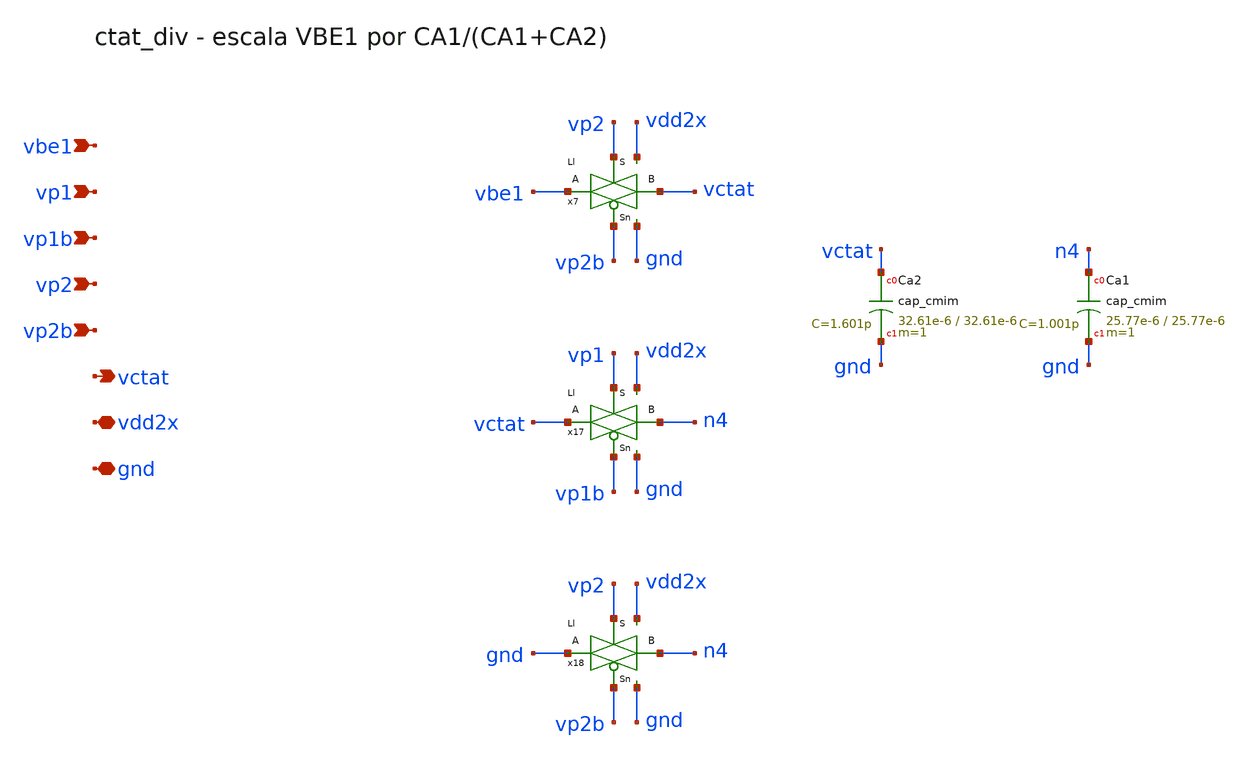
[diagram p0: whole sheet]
** sch_path: Enfoque_A/xschem/celdas/ctat_div.sch
**.subckt ctat_div vbe1 vp1 vp1b vp2 vp2b vctat vdd2x gnd
*.ipin vbe1
*.ipin vp1
*.ipin vp1b
*.ipin vp2
*.ipin vp2b
*.opin vctat
*.iopin vdd2x
*.iopin gnd
x7 vbe1 vctat vp2 vp2b vdd2x gnd Ll
x17 vctat n4 vp1 vp1b vdd2x gnd Ll
x18 gnd n4 vp2 vp2b vdd2x gnd Ll
XCa2 vctat gnd cap_cmim w=32.61e-6 l=32.61e-6 m=1 mm_ok=1
XCa1 n4 gnd cap_cmim w=25.77e-6 l=25.77e-6 m=1 mm_ok=1
**.ends

* expanding   symbol:  Enfoque_A/xschem/celdas/Ll.sym # of pins=6
** sym_path: Enfoque_A/xschem/celdas/Ll.sym
** sch_path: Enfoque_A/xschem/celdas/Ll.sch
.subckt Ll A B S Sn vdd gnd
*.iopin gnd
*.iopin vdd
*.iopin B
*.ipin Sn
*.ipin S
*.iopin A
XM101 A S B gnd sg13_lv_nmos w=0.13u l=0.130u ng=1 m=1 mm_ok=1
XM100 B Sn A vdd sg13_lv_pmos w=0.3u l=0.130u ng=1 m=1 mm_ok=1
.ends

.end
